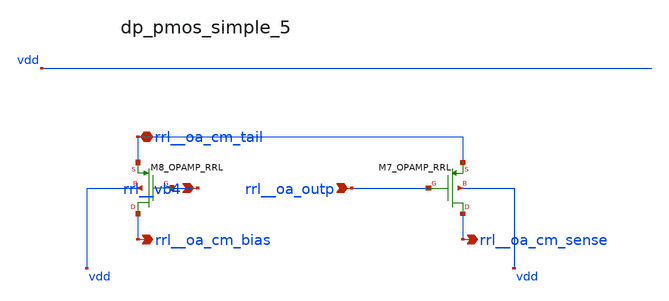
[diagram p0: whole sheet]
** sch_path: analog-db/raw/ia_004_fan_chopper_rrl/hier/blocks/dp_pmos_simple_5.sch
**.subckt dp_pmos_simple_5 rrl__vb4 rrl__oa_outp rrl__oa_cm_tail rrl__oa_cm_bias rrl__oa_cm_sense
*.ipin rrl__vb4
*.ipin rrl__oa_outp
*.iopin rrl__oa_cm_tail
*.opin rrl__oa_cm_bias
*.opin rrl__oa_cm_sense
XM7_OPAMP_RRL rrl__oa_cm_sense rrl__oa_outp rrl__oa_cm_tail vdd sg13_lv_pmos w=x_dut_xm7_opamp_rrl_w
+ l=x_dut_xm7_opamp_rrl_l ng=1 m=x_dut_xm7_opamp_rrl_m
XM8_OPAMP_RRL rrl__oa_cm_bias rrl__vb4 rrl__oa_cm_tail vdd sg13_lv_pmos w=x_dut_xm8_opamp_rrl_w
+ l=x_dut_xm8_opamp_rrl_l ng=1 m=x_dut_xm8_opamp_rrl_m
**.ends
.end
